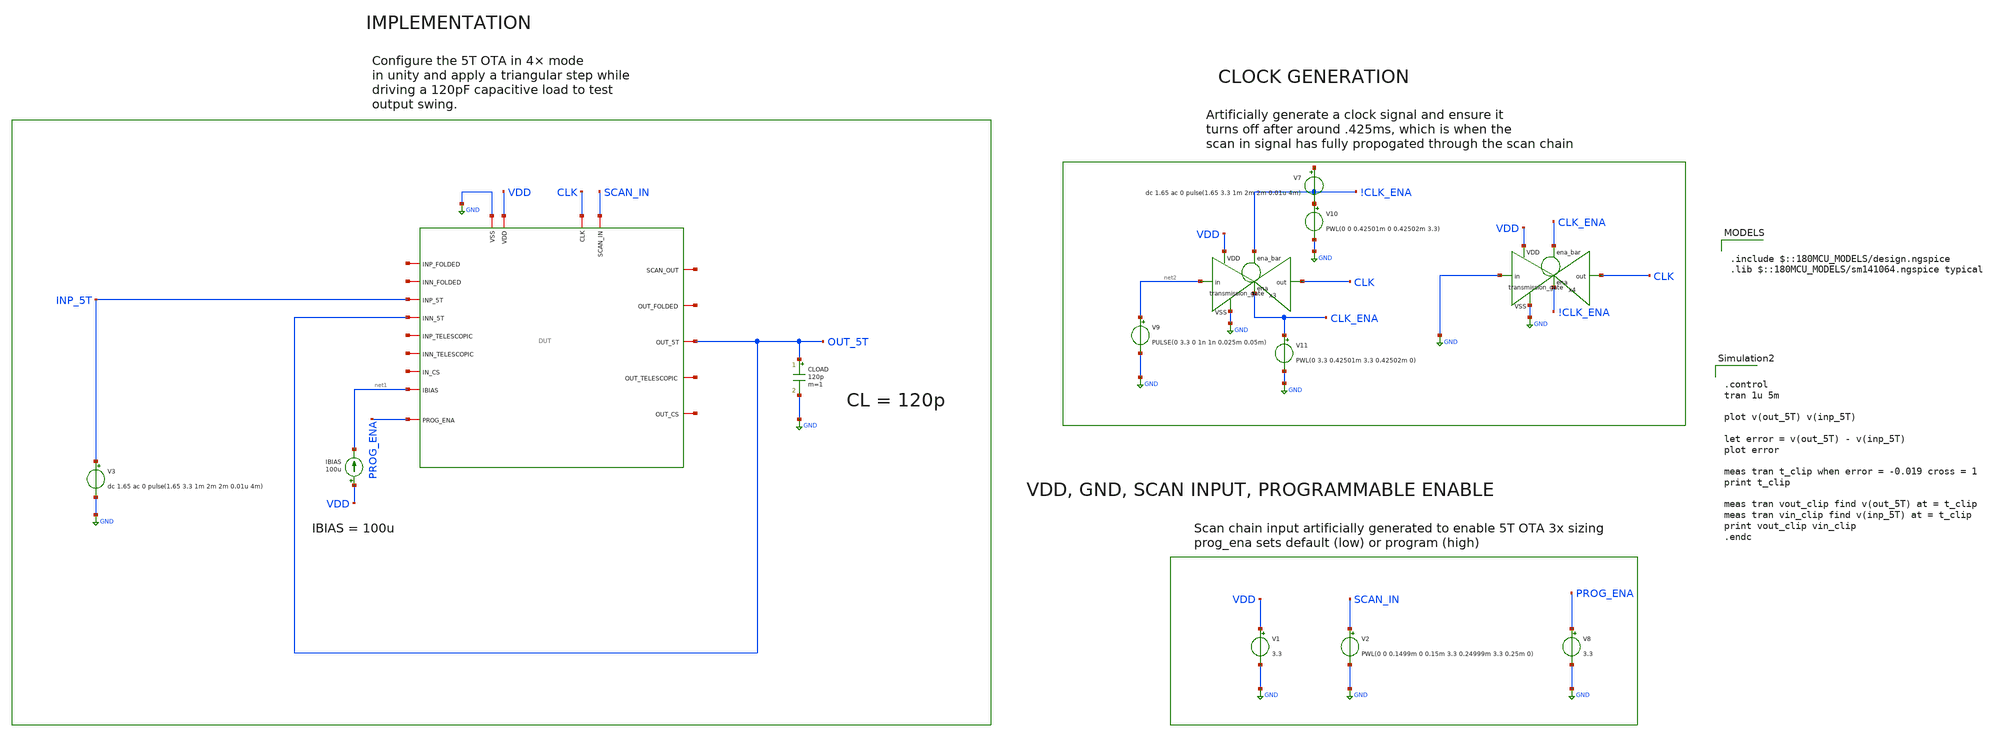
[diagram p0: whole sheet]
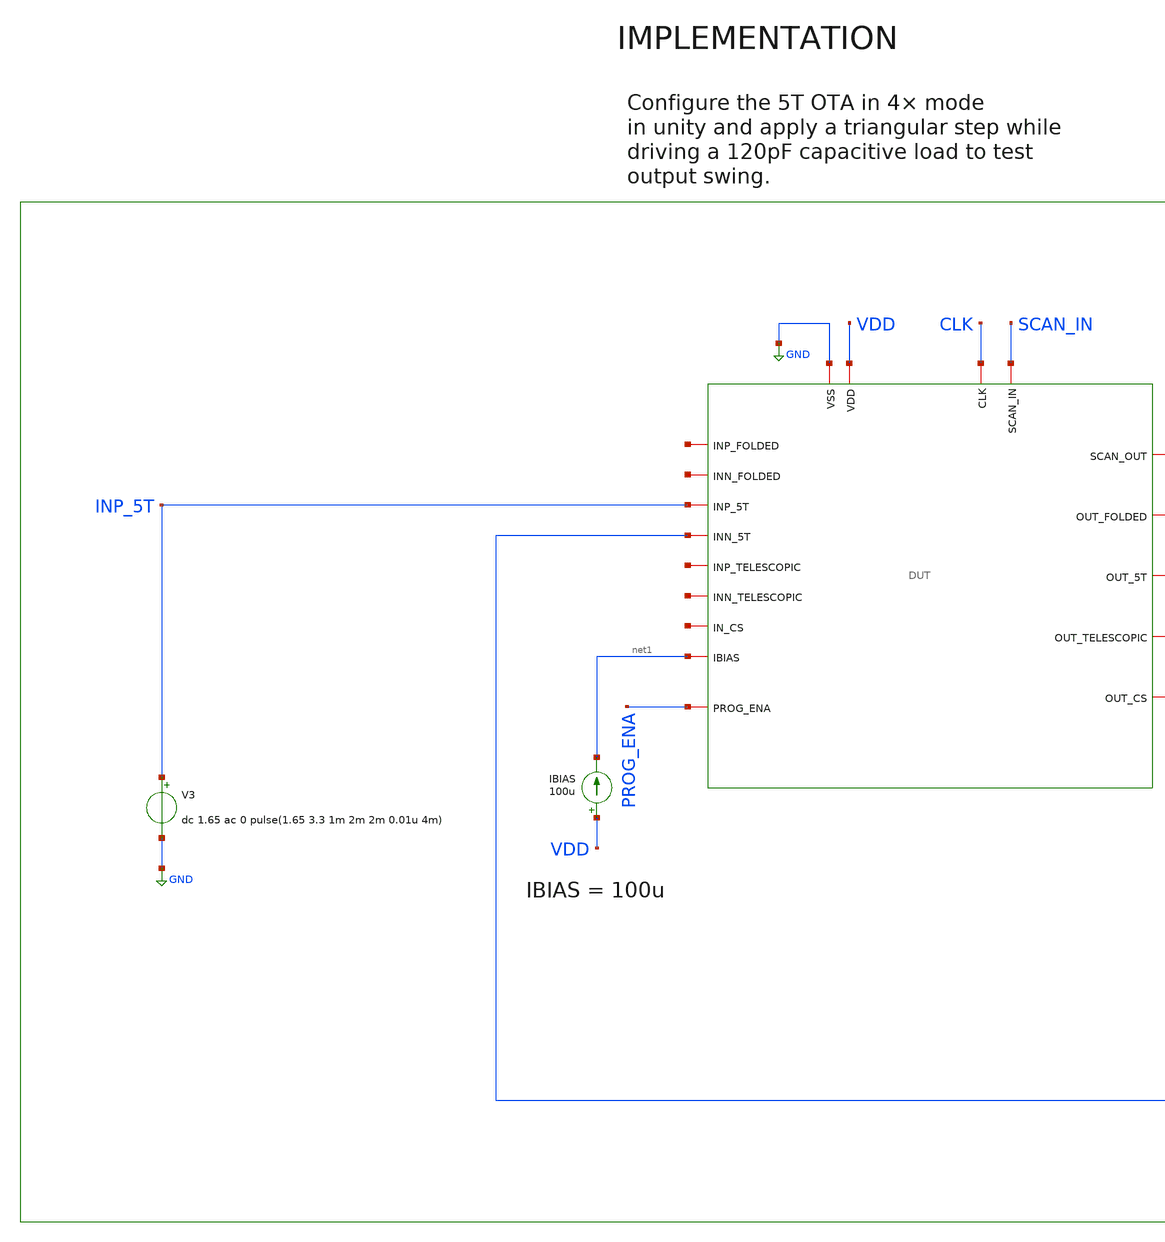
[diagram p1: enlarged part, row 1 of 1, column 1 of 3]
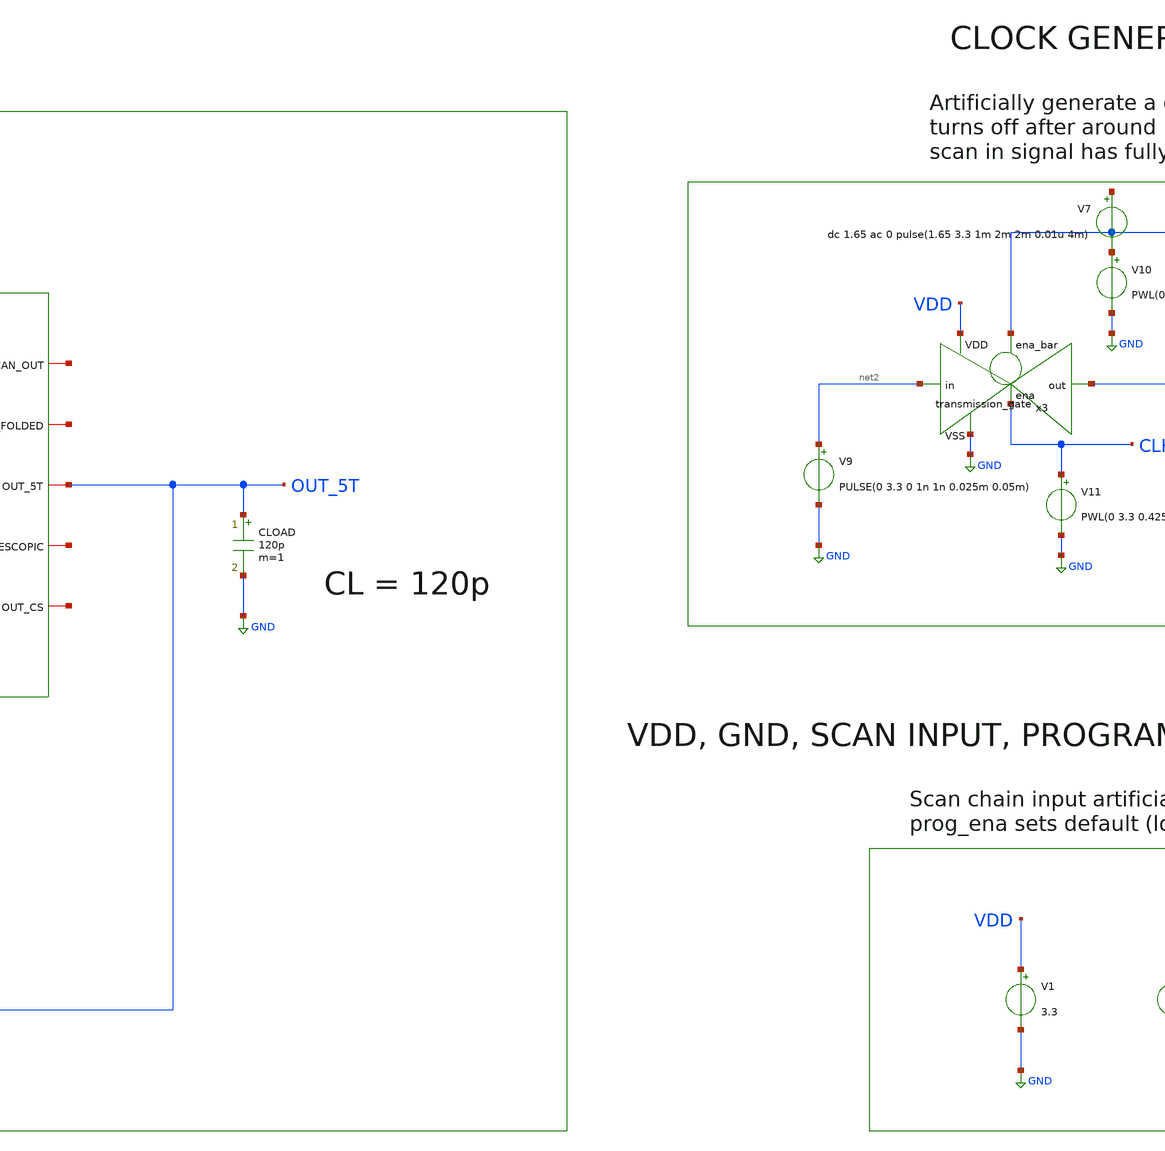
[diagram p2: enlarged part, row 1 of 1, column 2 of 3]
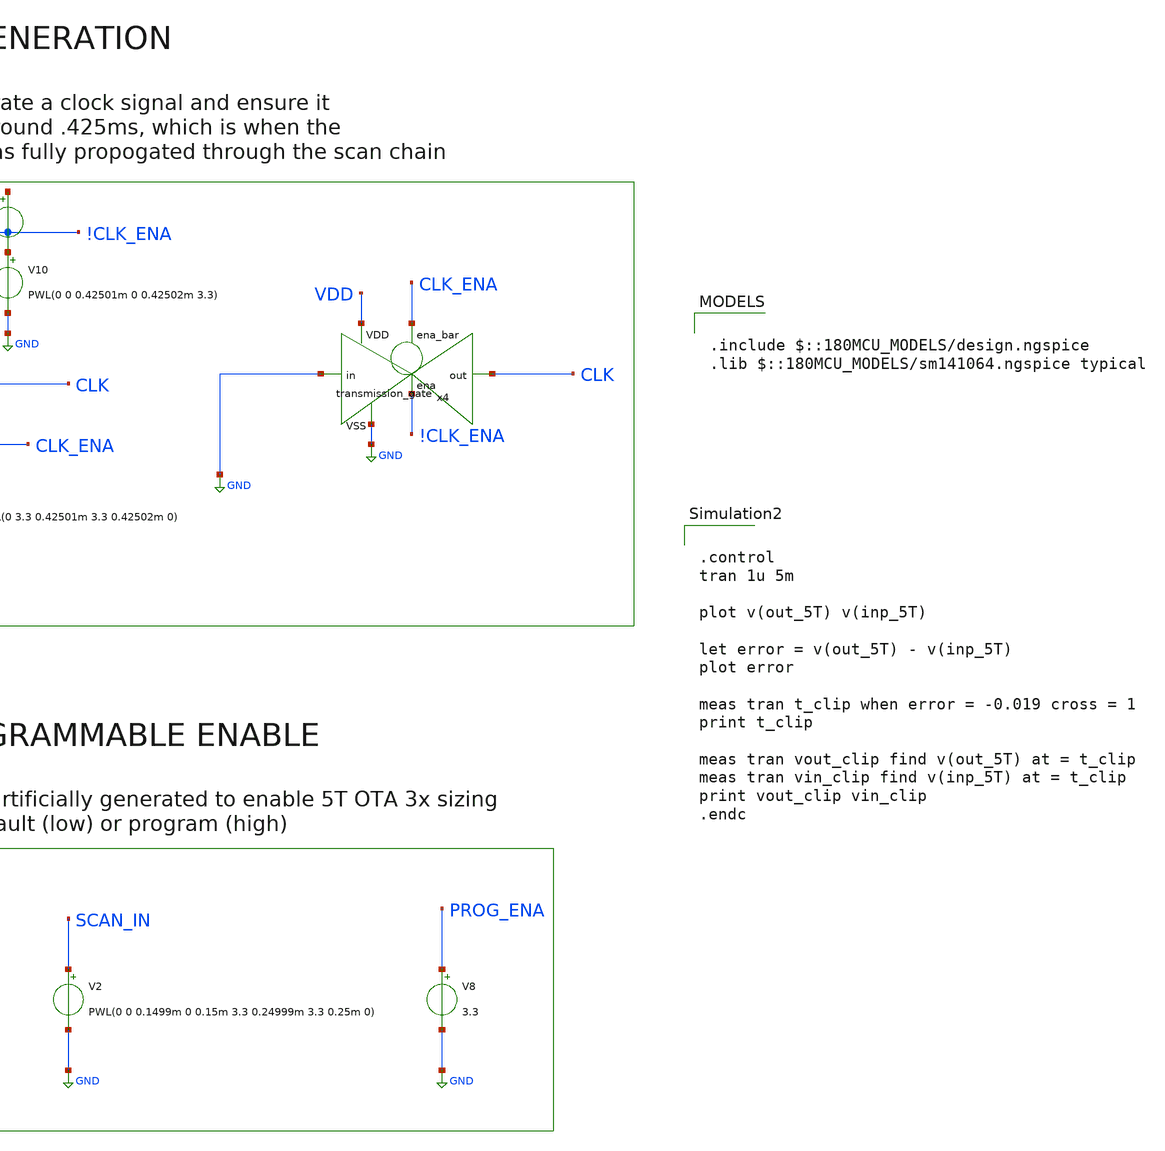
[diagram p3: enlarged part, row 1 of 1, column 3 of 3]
** sch_path: designs/libs/verification/ota_5t/4x_sizing/5t_4x_large_signal_upper_swing_tb.sch
**.subckt 5t_4x_large_signal_upper_swing_tb
V1 VDD GND 3.3
IBIAS VDD net1 100u
CLOAD OUT_5T GND 120p m=1
x1 CLK net3 SCAN_IN GND VDD net4 net5 OUT_5T net1 net6 INP_5T OUT_5T net7 net8 net9 net10 net11
+ PROG_ENA DUT
V8 PROG_ENA GND 3.3
V9 net2 GND PULSE(0 3.3 0 1n 1n 0.025m 0.05m)
x3 !CLK_ENA VDD CLK net2 GND CLK_ENA transmission_gate
V10 !CLK_ENA GND PWL(0 0 0.42501m 0 0.42502m 3.3)
V11 CLK_ENA GND PWL(0 3.3 0.42501m 3.3 0.42502m 0)
x4 CLK_ENA VDD CLK GND GND !CLK_ENA transmission_gate
V2 SCAN_IN GND PWL(0 0 0.1499m 0 0.15m 3.3 0.24999m 3.3 0.25m 0)
V7 net12 !CLK_ENA dc 1.65 ac 0 pulse(1.65 3.3 1m 2m 2m 0.01u 4m)
V3 INP_5T GND dc 1.65 ac 0 pulse(1.65 3.3 1m 2m 2m 0.01u 4m)
**** begin user architecture code

.include $::180MCU_MODELS/design.ngspice
.lib $::180MCU_MODELS/sm141064.ngspice typical



.control
tran 1u 5m

plot v(out_5T) v(inp_5T)

let error = v(out_5T) - v(inp_5T)
plot error

meas tran t_clip when error = -0.019 cross = 1
print t_clip

meas tran vout_clip find v(out_5T) at = t_clip
meas tran vin_clip find v(inp_5T) at = t_clip
print vout_clip vin_clip
.endc


**** end user architecture code
**.ends
.GLOBAL GND
.end
